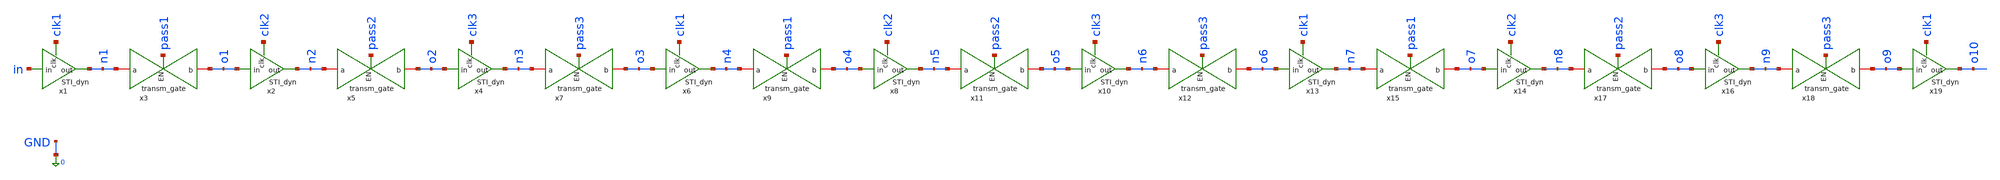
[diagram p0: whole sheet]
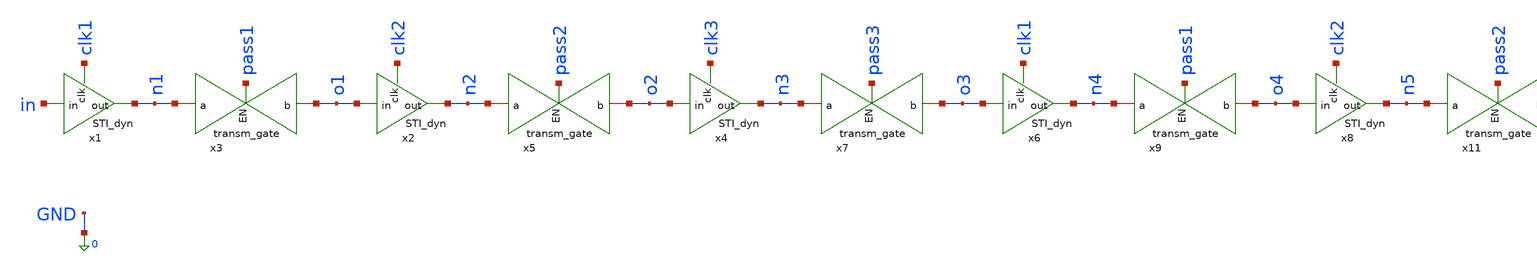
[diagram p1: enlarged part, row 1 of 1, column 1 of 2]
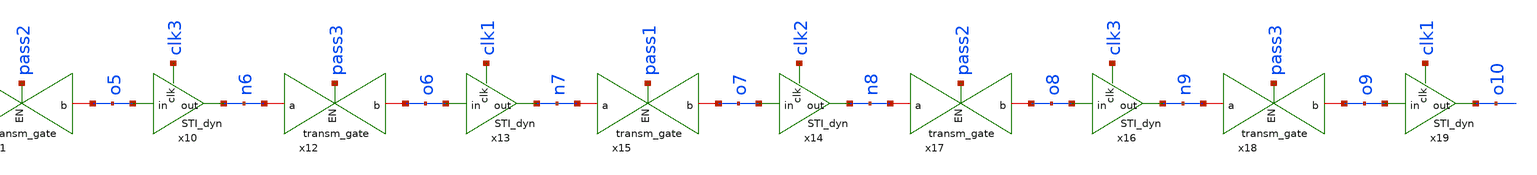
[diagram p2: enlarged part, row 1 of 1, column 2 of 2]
** sch_path: xschem_designs/STI_dyn_TB.sch
**.subckt STI_dyn_TB
x1 clk1 in n1 STI_dyn
x2 clk2 o1 n2 STI_dyn
x3 n1 o1 pass1 transm_gate
x4 clk3 o2 n3 STI_dyn
x5 n2 o2 pass2 transm_gate
x7 n3 o3 pass3 transm_gate
x6 clk1 o3 n4 STI_dyn
x8 clk2 o4 n5 STI_dyn
x9 n4 o4 pass1 transm_gate
x10 clk3 o5 n6 STI_dyn
x11 n5 o5 pass2 transm_gate
x12 n6 o6 pass3 transm_gate
x13 clk1 o6 n7 STI_dyn
x14 clk2 o7 n8 STI_dyn
x15 n7 o7 pass1 transm_gate
x16 clk3 o8 n9 STI_dyn
x17 n8 o8 pass2 transm_gate
x18 n9 o9 pass3 transm_gate
x19 clk1 o9 o10 STI_dyn
**** begin user architecture code


.global VDD GND BP BN
.option temp=27
.include /usr/local/share/pdk/gf180mcuC/libs.tech/ngspice/design.ngspice
.lib /usr/local/share/pdk/gf180mcuC/libs.tech/ngspice/sm141064.ngspice statistical

Vdd VDD 0 3.3
Vbp BP VDD 2.7
Vbn BN GND -2.7
Vin in 0 PWL(0 0 10u 3.3)
Vclk1 clk1 0 PULSE(0 3.3 0 100p 100p 20n 60n)
Vpass1 pass1 0 PULSE(0 3.3 -20n 100p 100p 40n 60n)
Vclk2 clk2 0 PULSE(0 3.3 20n 100p 100p 20n 60n)
Vpass2 pass2 0 PULSE(0 3.3 0n 100p 100p 40n 60n)
Vclk3 clk3 0 PULSE(0 3.3 -20n 100p 100p 20n 60n)
Vpass3 pass3 0 PULSE(0 3.3 20n 100p 100p 40n 60n)

.param sw_stat_global = 1
.param sw_stat_mismatch = 1

.control
  let runs = 1000
  let run = 1

  option seed = 12345
  save v(o10) v(clk1)
  dowhile run <= runs
    tran 0.1n 10u
    linearize
    wrdata MC/STI_dyn/STI_dyn_TB{$&run}.txt v(o10) v(clk1)
    reset
    let run = run + 1
  end

.endc


**** end user architecture code
**.ends

* expanding   symbol:  xschem_designs/STI_dyn.sym # of pins=3
** sym_path: xschem_designs/STI_dyn.sym
** sch_path: xschem_designs/STI_dyn.sch
.subckt STI_dyn clk in out
*.ipin in
*.opin out
*.ipin clk
XM4 out clk VDD VDD pfet_03v3 L=0.28u W=0.88u nf=1 ad='int((nf+1)/2) * W/nf * 0.18u' as='int((nf+2)/2) * W/nf * 0.18u'
+ pd='2*int((nf+1)/2) * (W/nf + 0.18u)' ps='2*int((nf+2)/2) * (W/nf + 0.18u)' nrd='0.18u / W' nrs='0.18u / W'
+ sa=0 sb=0 sd=0 m=1 par=1
XM7 out out net3 GND nfet_03v3 L=0.28u W=0.22u nf=1 ad='int((nf+1)/2) * W/nf * 0.18u' as='int((nf+2)/2) * W/nf * 0.18u'
+ pd='2*int((nf+1)/2) * (W/nf + 0.18u)' ps='2*int((nf+2)/2) * (W/nf + 0.18u)' nrd='0.18u / W' nrs='0.18u / W'
+ sa=0 sb=0 sd=0 m=1 par=1
XM2 net3 net3 net2 GND nfet_03v3 L=0.28u W=0.22u nf=1 ad='int((nf+1)/2) * W/nf * 0.18u' as='int((nf+2)/2) * W/nf * 0.18u'
+ pd='2*int((nf+1)/2) * (W/nf + 0.18u)' ps='2*int((nf+2)/2) * (W/nf + 0.18u)' nrd='0.18u / W' nrs='0.18u / W'
+ sa=0 sb=0 sd=0 m=1 par=1
XM8 net2 in net1 GND nfet_03v3 L=0.28u W=0.22u nf=1 ad='int((nf+1)/2) * W/nf * 0.18u' as='int((nf+2)/2) * W/nf * 0.18u'
+ pd='2*int((nf+1)/2) * (W/nf + 0.18u)' ps='2*int((nf+2)/2) * (W/nf + 0.18u)' nrd='0.18u / W' nrs='0.18u / W'
+ sa=0 sb=0 sd=0 m=1 par=1
XM9 out in net1 BN nfet_06v0 L=0.70u W=0.30u nf=1 ad='int((nf+1)/2) * W/nf * 0.18u' as='int((nf+2)/2) * W/nf * 0.18u'
+ pd='2*int((nf+1)/2) * (W/nf + 0.18u)' ps='2*int((nf+2)/2) * (W/nf + 0.18u)' nrd='0.18u / W' nrs='0.18u / W'
+ sa=0 sb=0 sd=0 m=1 par=1
XM10 net1 clk GND GND nfet_03v3 L=0.28u W=0.22u nf=1 ad='int((nf+1)/2) * W/nf * 0.18u' as='int((nf+2)/2) * W/nf * 0.18u'
+ pd='2*int((nf+1)/2) * (W/nf + 0.18u)' ps='2*int((nf+2)/2) * (W/nf + 0.18u)' nrd='0.18u / W' nrs='0.18u / W'
+ sa=0 sb=0 sd=0 m=1 par=1
.ends


* expanding   symbol:  xschem_designs/transm_gate.sym # of pins=3
** sym_path: xschem_designs/transm_gate.sym
** sch_path: xschem_designs/transm_gate.sch
.subckt transm_gate a b EN
*.iopin b
*.iopin a
*.ipin EN
XM1 net1 EN GND GND nfet_03v3 L=0.28u W=0.22u nf=1 ad='int((nf+1)/2) * W/nf * 0.18u' as='int((nf+2)/2) * W/nf * 0.18u'
+ pd='2*int((nf+1)/2) * (W/nf + 0.18u)' ps='2*int((nf+2)/2) * (W/nf + 0.18u)' nrd='0.18u / W' nrs='0.18u / W'
+ sa=0 sb=0 sd=0 m=1 par=1
XM2 net1 EN VDD VDD pfet_03v3 L=0.28u W=0.44u nf=1 ad='int((nf+1)/2) * W/nf * 0.18u' as='int((nf+2)/2) * W/nf * 0.18u'
+ pd='2*int((nf+1)/2) * (W/nf + 0.18u)' ps='2*int((nf+2)/2) * (W/nf + 0.18u)' nrd='0.18u / W' nrs='0.18u / W'
+ sa=0 sb=0 sd=0 m=1 par=1
XM3 a net1 b VDD pfet_03v3 L=0.28u W=0.44u nf=1 ad='int((nf+1)/2) * W/nf * 0.18u' as='int((nf+2)/2) * W/nf * 0.18u'
+ pd='2*int((nf+1)/2) * (W/nf + 0.18u)' ps='2*int((nf+2)/2) * (W/nf + 0.18u)' nrd='0.18u / W' nrs='0.18u / W'
+ sa=0 sb=0 sd=0 m=1 par=1
XM4 a EN b GND nfet_03v3 L=0.28u W=0.22u nf=1 ad='int((nf+1)/2) * W/nf * 0.18u' as='int((nf+2)/2) * W/nf * 0.18u'
+ pd='2*int((nf+1)/2) * (W/nf + 0.18u)' ps='2*int((nf+2)/2) * (W/nf + 0.18u)' nrd='0.18u / W' nrs='0.18u / W'
+ sa=0 sb=0 sd=0 m=1 par=1
.ends

.end
